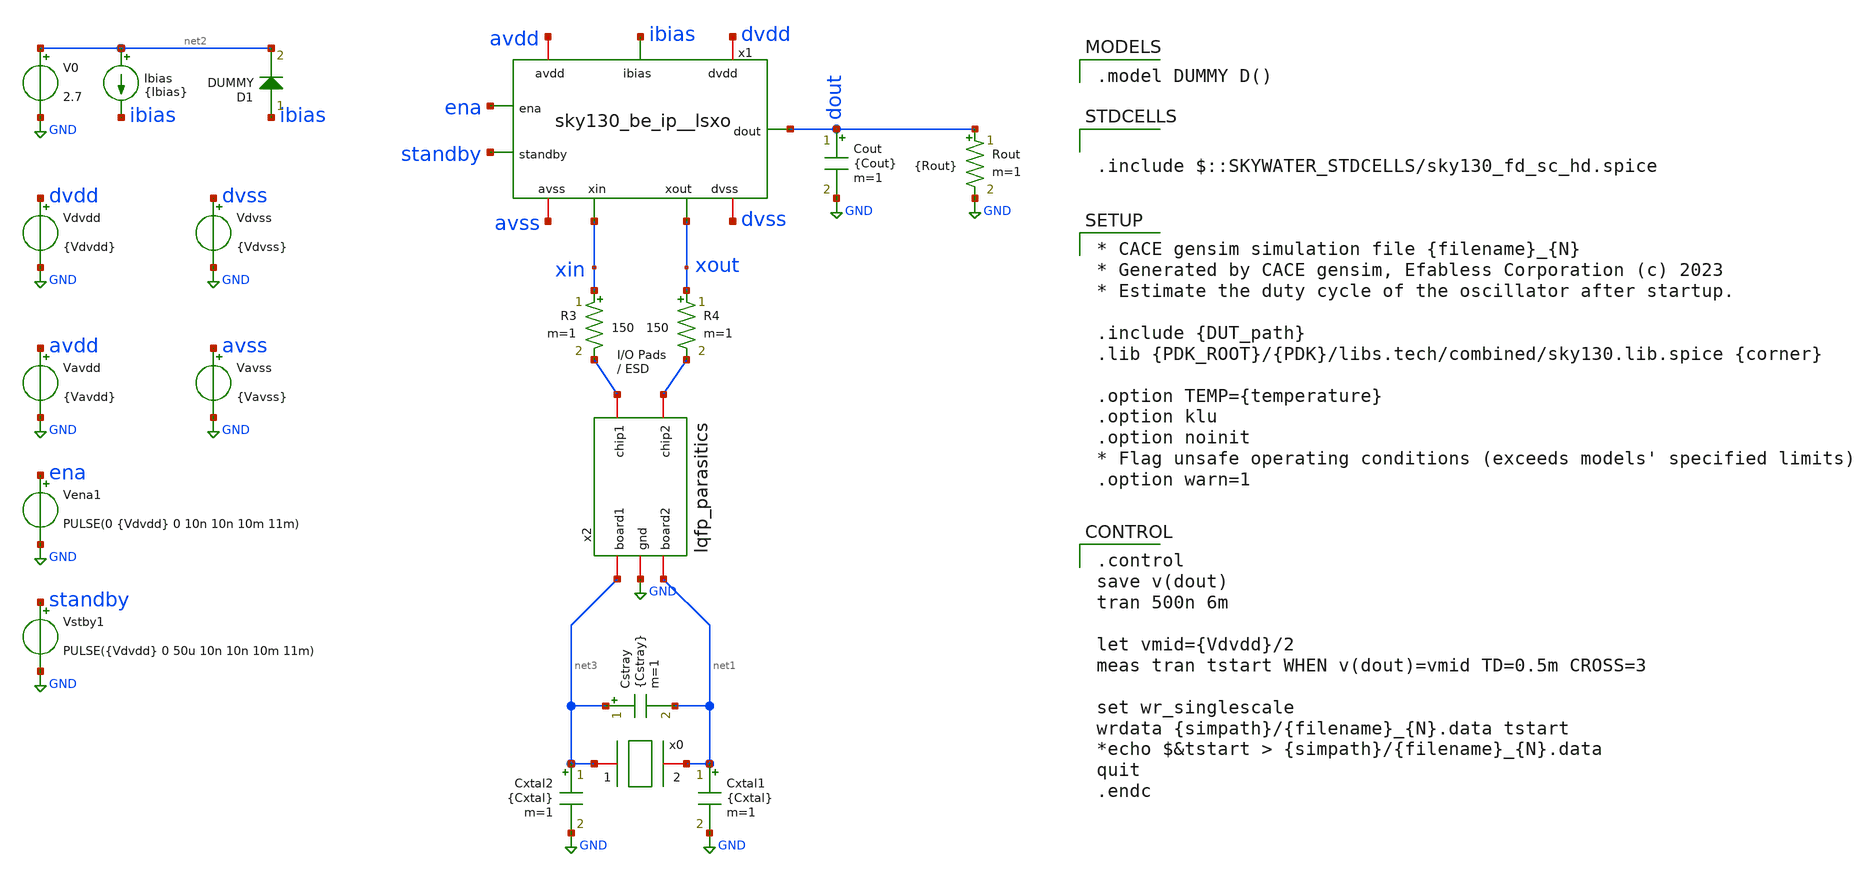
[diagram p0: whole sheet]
** sch_path: cace/templates/tb_startup_clk_on.sch

.include $::SKYWATER_STDCELLS/sky130_fd_sc_hd.spice

**.subckt tb_startup_clk_on
Vdvdd dvdd GND {Vdvdd}
Vavdd avdd GND {Vavdd}
Cxtal2 net3 GND {Cxtal} m=1
Cxtal1 net1 GND {Cxtal} m=1
Cstray net3 net1 {Cstray} m=1
Ibias net2 ibias {Ibias}
Cout dout GND {Cout} m=1
V0 net2 GND 2.7
R3 xin net4 150 m=1
R4 xout net5 150 m=1
x2 net5 net4 GND net3 net1 lqfp_parasitics
D1 ibias net2 DUMMY area=100
x1 avdd avss dvdd dvss ibias ena standby dout xin xout sky130_be_ip__lsxo
Vdvss dvss GND {Vdvss}
Vavss avss GND {Vavss}
Rout dout GND {Rout} m=1
x0 net3 net1 xtal_iqd_125_1
Vena1 ena GND PULSE(0 {Vdvdd} 0 10n 10n 10m 11m)
Vstby1 standby GND PULSE({Vdvdd} 0 50u 10n 10n 10m 11m)
**** begin user architecture code

.model DUMMY D()


.control
save v(dout)
tran 500n 6m

let vmid={Vdvdd}/2
meas tran tstart WHEN v(dout)=vmid TD=0.5m CROSS=3

set wr_singlescale
wrdata {simpath}/{filename}_{N}.data tstart
*echo $&tstart > {simpath}/{filename}_{N}.data
quit
.endc



* CACE gensim simulation file {filename}_{N}
* Generated by CACE gensim, Efabless Corporation (c) 2023
* Estimate the duty cycle of the oscillator after startup.

.include {DUT_path}
.lib {PDK_ROOT}/{PDK}/libs.tech/combined/sky130.lib.spice {corner}

.option TEMP={temperature}
.option klu
.option noinit
* Flag unsafe operating conditions (exceeds models' specified limits)
.option warn=1


**** end user architecture code
**.ends
.GLOBAL GND
.end
